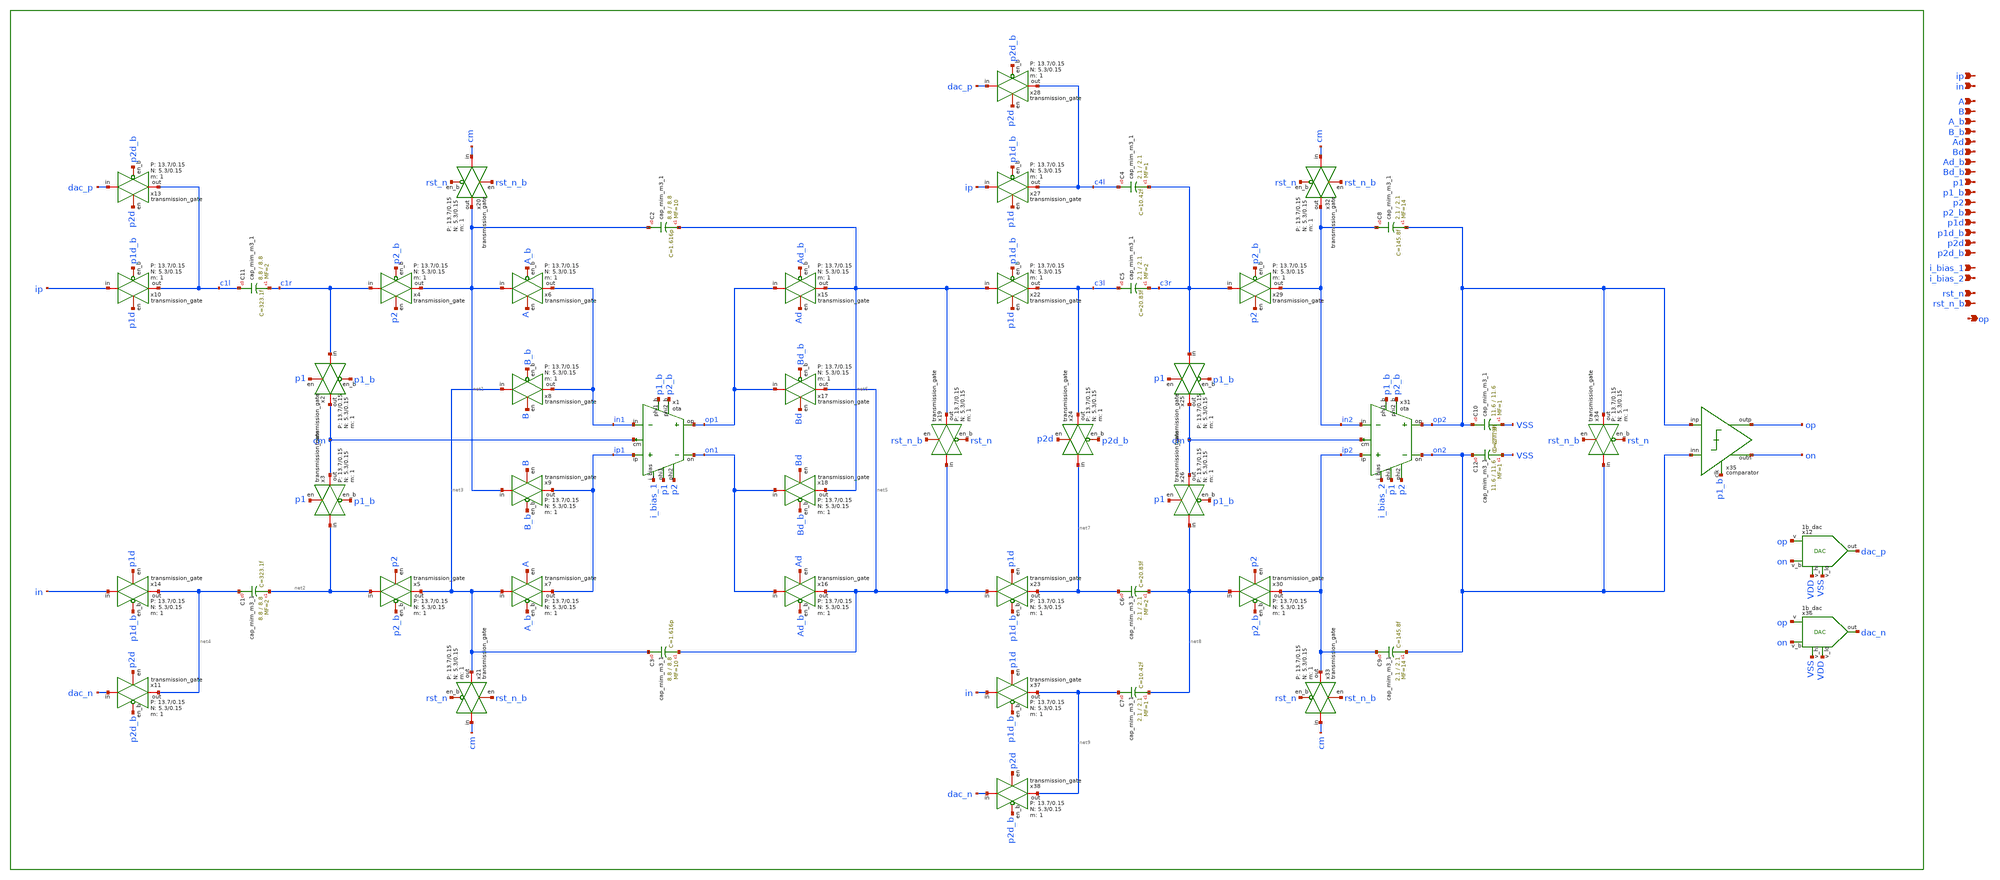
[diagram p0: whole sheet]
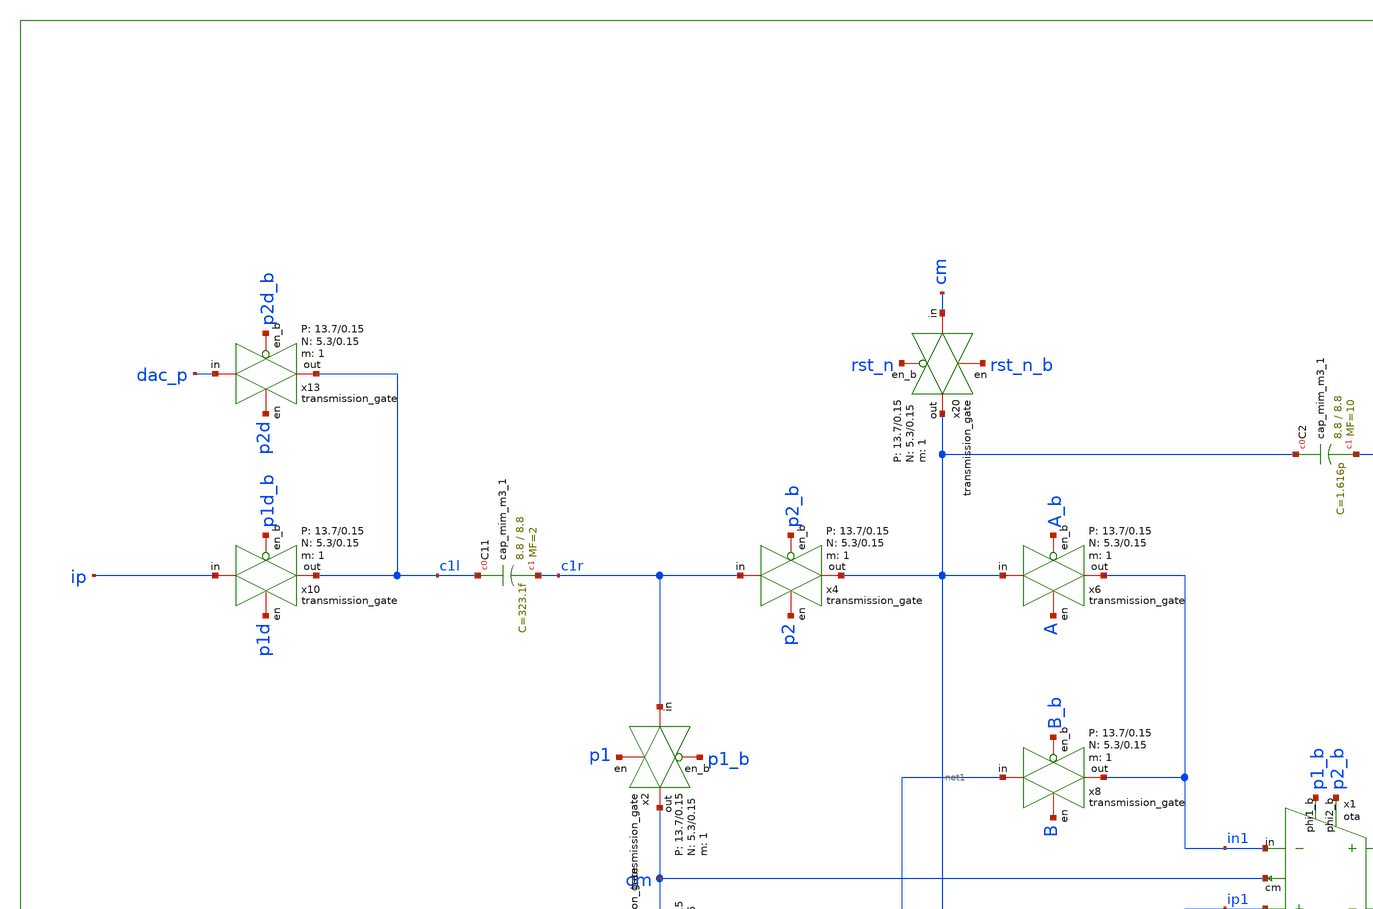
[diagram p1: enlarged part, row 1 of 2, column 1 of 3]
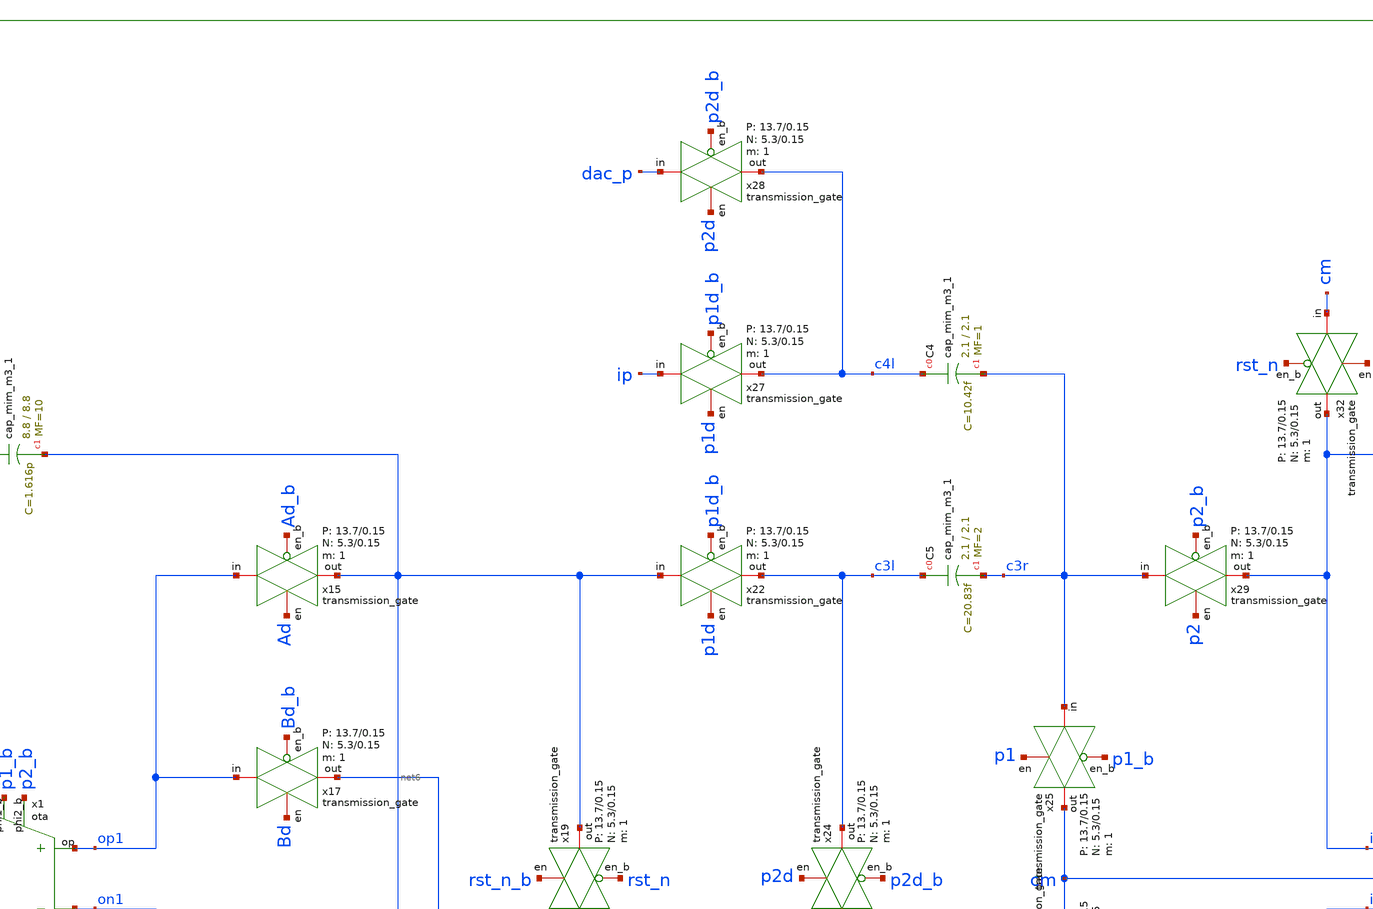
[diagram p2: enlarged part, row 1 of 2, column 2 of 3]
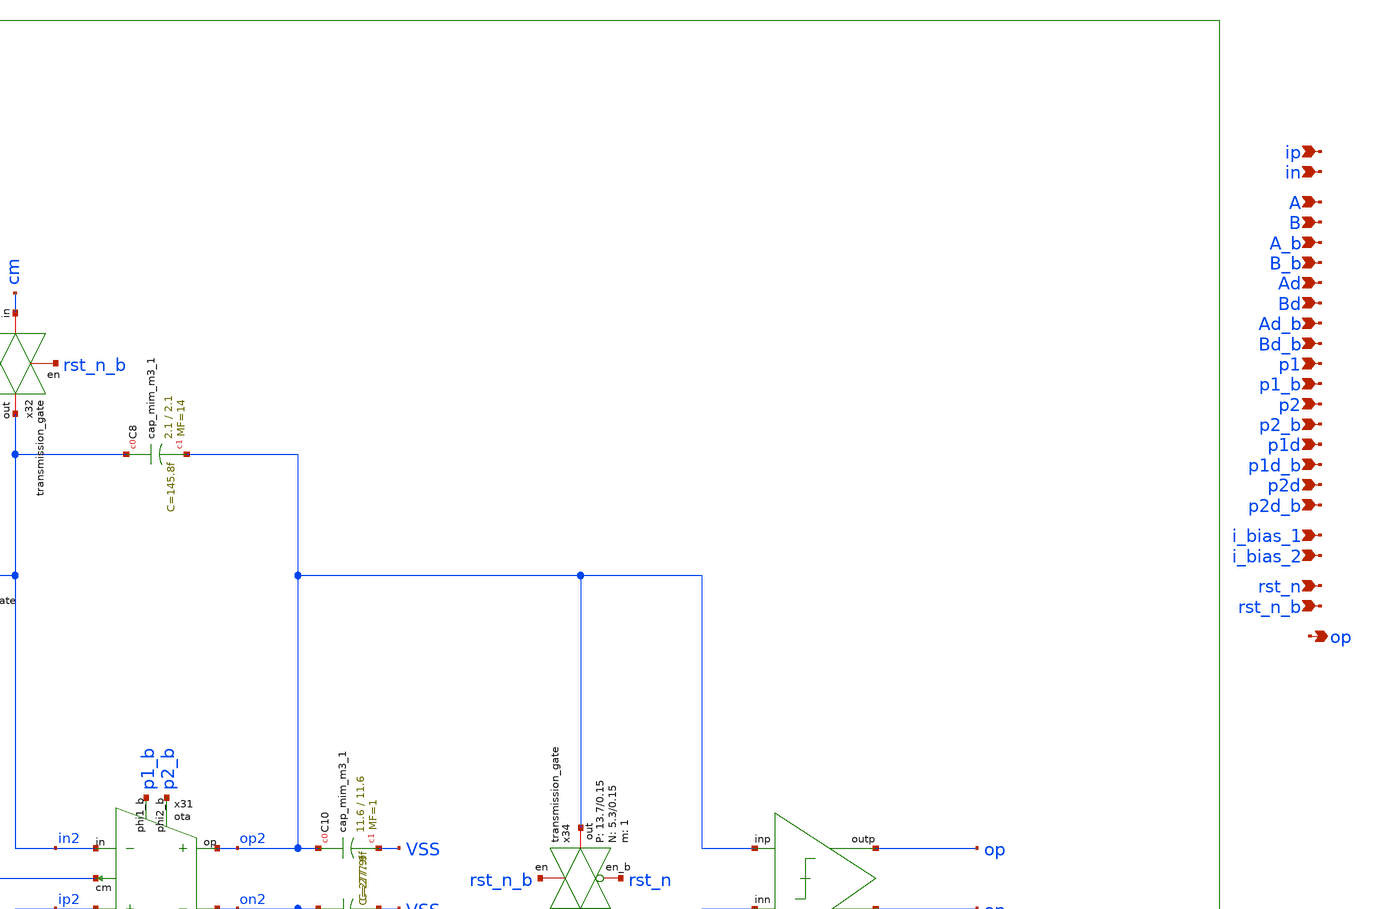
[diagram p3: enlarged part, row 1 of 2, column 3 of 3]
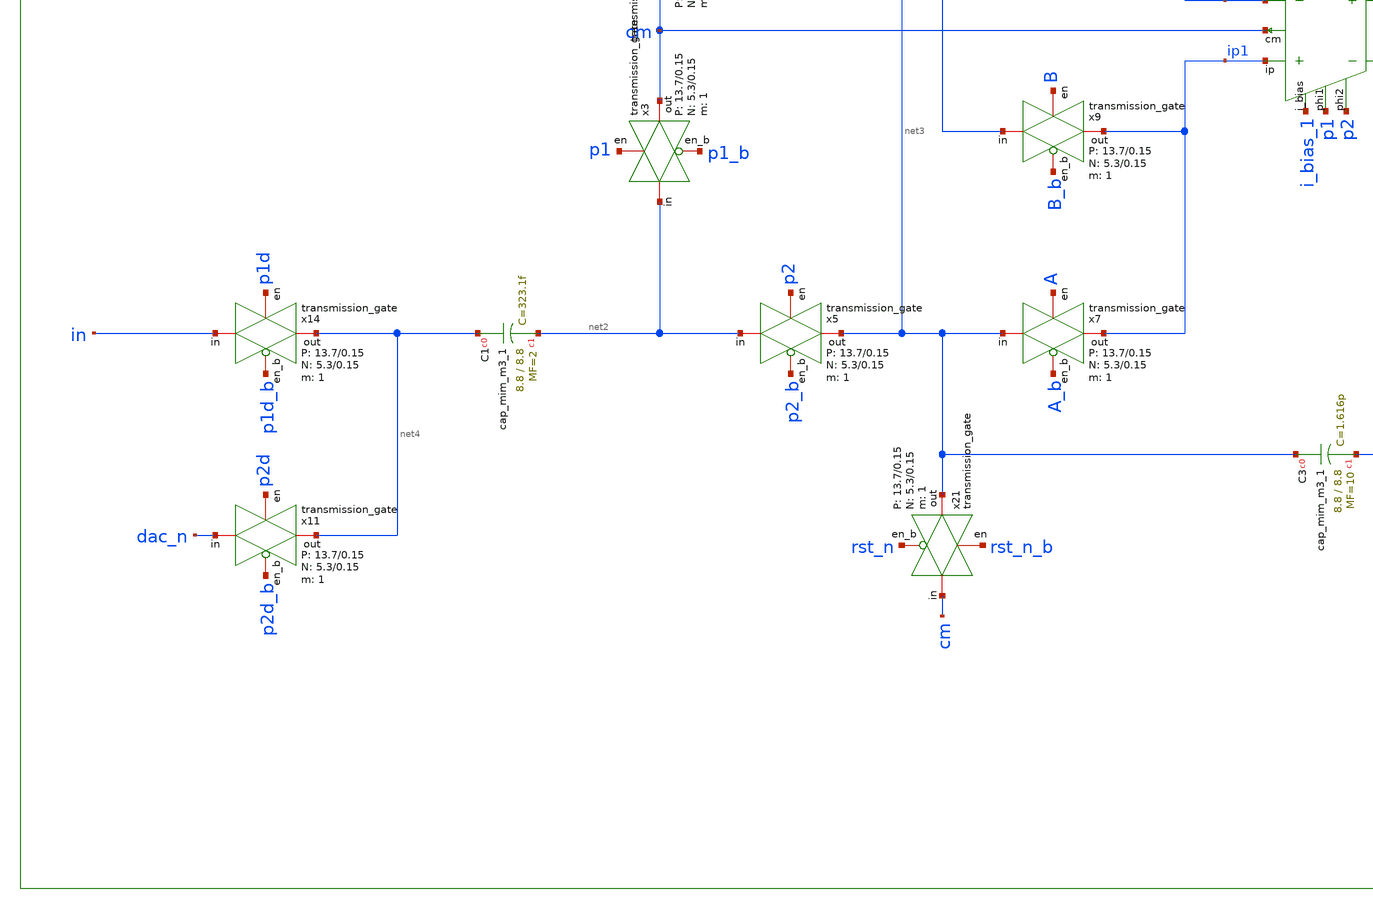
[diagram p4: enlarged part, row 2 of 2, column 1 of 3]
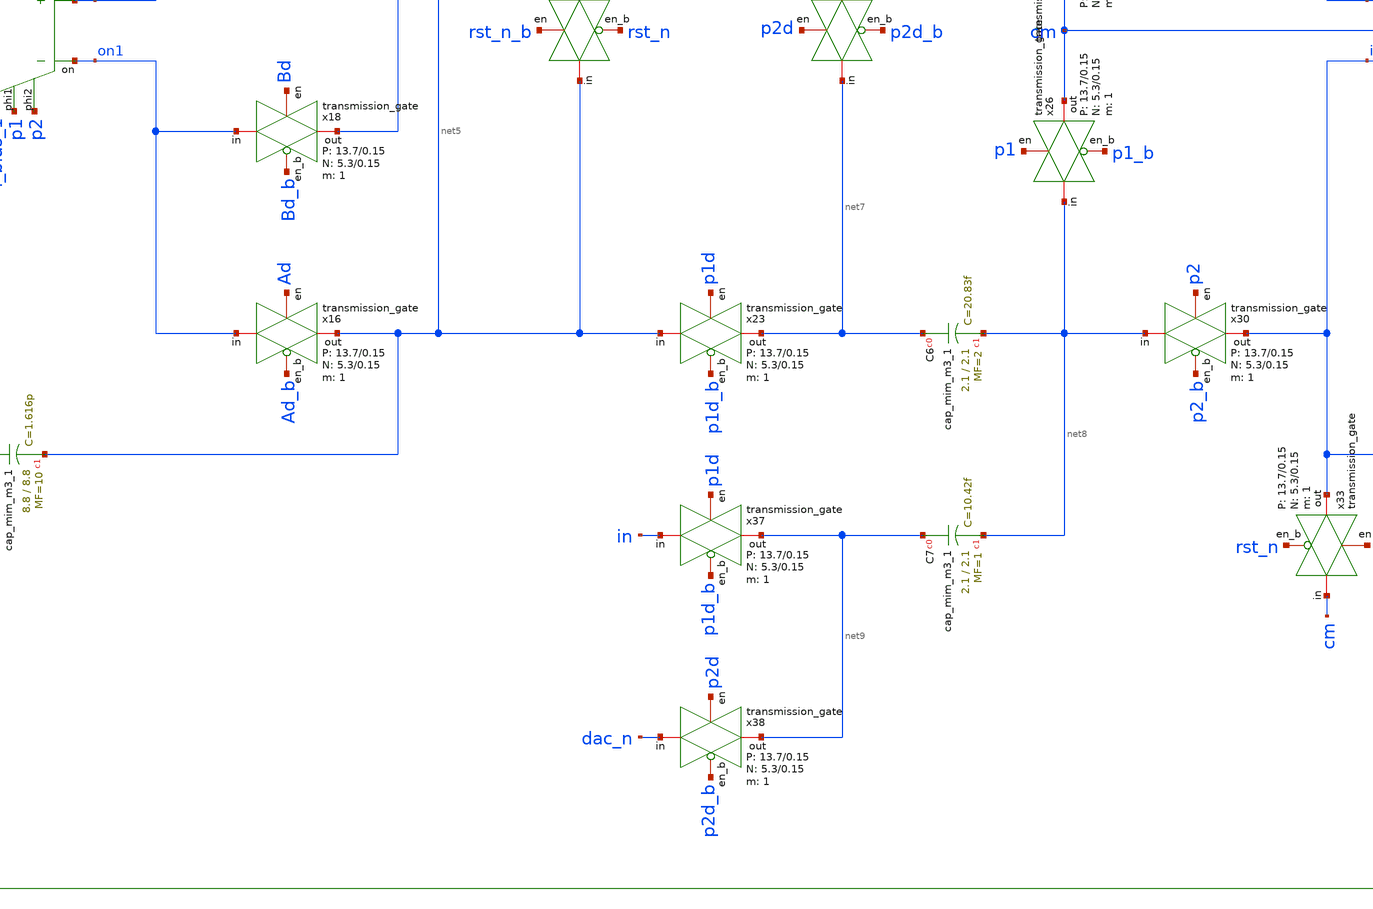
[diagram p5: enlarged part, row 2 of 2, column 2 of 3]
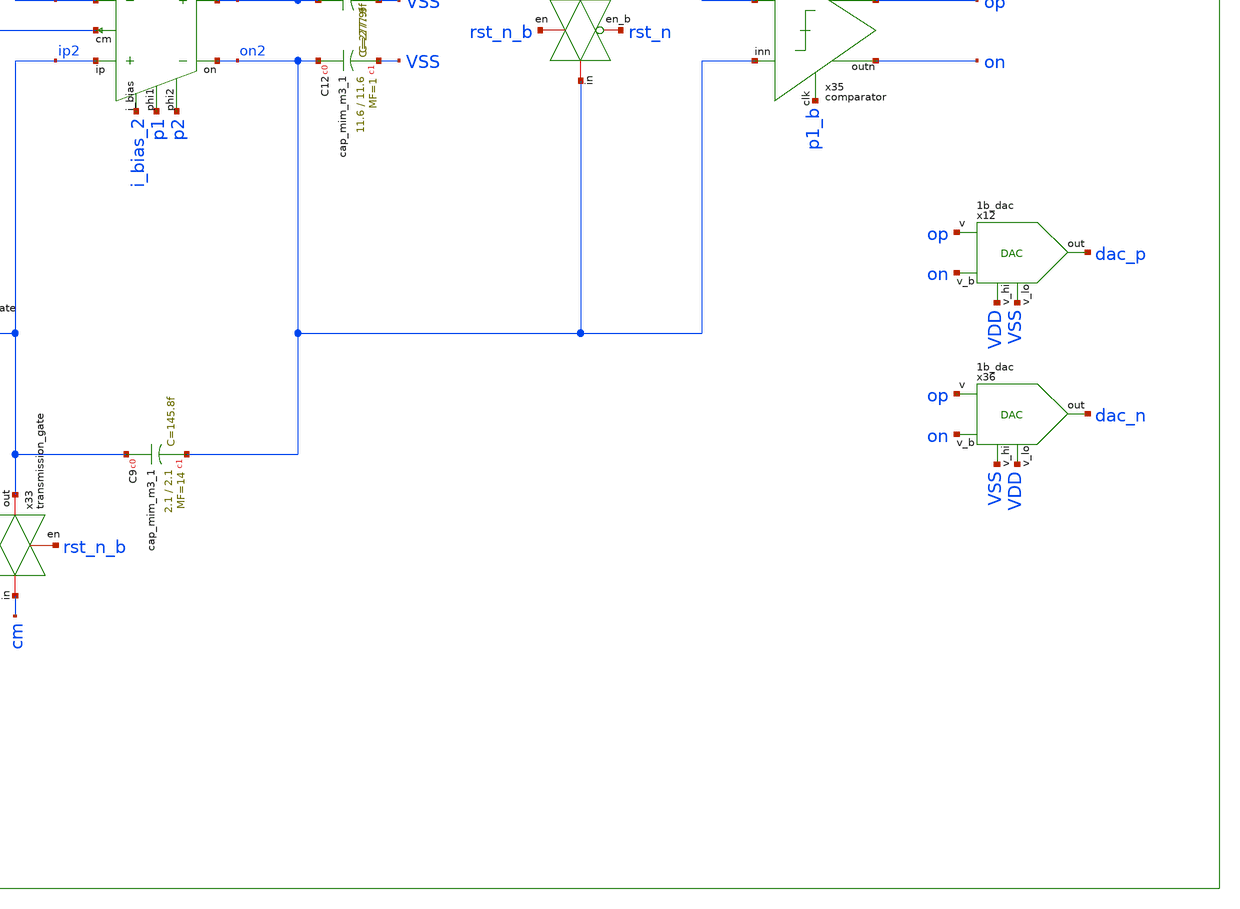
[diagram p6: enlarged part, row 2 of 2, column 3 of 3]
** sch_path: design/analog_modulator/schematic/modulator_backup.sch
**.subckt modulator_backup ip in A B A_b B_b Ad Bd Ad_b Bd_b p1 p1_b p2 p2_b p1d p1d_b p2d p2d_b
*+ i_bias_1 i_bias_2 rst_n rst_n_b op
*.ipin ip
*.ipin in
*.ipin A
*.ipin B
*.ipin A_b
*.ipin B_b
*.ipin Ad
*.ipin Bd
*.ipin Ad_b
*.ipin Bd_b
*.ipin p1
*.ipin p1_b
*.ipin p2
*.ipin p2_b
*.ipin p1d
*.ipin p1d_b
*.ipin p2d
*.ipin p2d_b
*.ipin i_bias_1
*.ipin i_bias_2
*.ipin rst_n
*.ipin rst_n_b
*.opin op
x1 i_bias_1 ip1 in1 p1 p1_b p2 p2_b op1 on1 cm VDD VSS ota
x4 c1r net1 p2 p2_b VDD VSS transmission_gate N=1 W_N=5.3 L_N=0.15 W_P=13.7 L_P=0.15
x5 net2 net3 p2 p2_b VDD VSS transmission_gate N=1 W_N=5.3 L_N=0.15 W_P=13.7 L_P=0.15
x2 c1r cm p1 p1_b VDD VSS transmission_gate N=1 W_N=5.3 L_N=0.15 W_P=13.7 L_P=0.15
x3 net2 cm p1 p1_b VDD VSS transmission_gate N=1 W_N=5.3 L_N=0.15 W_P=13.7 L_P=0.15
x10 ip c1l p1d p1d_b VDD VSS transmission_gate N=1 W_N=5.3 L_N=0.15 W_P=13.7 L_P=0.15
x11 dac_n net4 p2d p2d_b VDD VSS transmission_gate N=1 W_N=5.3 L_N=0.15 W_P=13.7 L_P=0.15
x12 VDD VSS op dac_p on VDD VSS 1b_dac
x13 dac_p c1l p2d p2d_b VDD VSS transmission_gate N=1 W_N=5.3 L_N=0.15 W_P=13.7 L_P=0.15
x14 in net4 p1d p1d_b VDD VSS transmission_gate N=1 W_N=5.3 L_N=0.15 W_P=13.7 L_P=0.15
x19 net5 net6 rst_n_b rst_n VDD VSS transmission_gate N=1 W_N=5.3 L_N=0.15 W_P=13.7 L_P=0.15
x20 cm net1 rst_n_b rst_n VDD VSS transmission_gate N=1 W_N=5.3 L_N=0.15 W_P=13.7 L_P=0.15
x21 cm net3 rst_n_b rst_n VDD VSS transmission_gate N=1 W_N=5.3 L_N=0.15 W_P=13.7 L_P=0.15
x22 net6 c3l p1d p1d_b VDD VSS transmission_gate N=1 W_N=5.3 L_N=0.15 W_P=13.7 L_P=0.15
x23 net5 net7 p1d p1d_b VDD VSS transmission_gate N=1 W_N=5.3 L_N=0.15 W_P=13.7 L_P=0.15
x24 net7 c3l p2d p2d_b VDD VSS transmission_gate N=1 W_N=5.3 L_N=0.15 W_P=13.7 L_P=0.15
x25 c3r cm p1 p1_b VDD VSS transmission_gate N=1 W_N=5.3 L_N=0.15 W_P=13.7 L_P=0.15
x26 net8 cm p1 p1_b VDD VSS transmission_gate N=1 W_N=5.3 L_N=0.15 W_P=13.7 L_P=0.15
x27 ip c4l p1d p1d_b VDD VSS transmission_gate N=1 W_N=5.3 L_N=0.15 W_P=13.7 L_P=0.15
x28 dac_p c4l p2d p2d_b VDD VSS transmission_gate N=1 W_N=5.3 L_N=0.15 W_P=13.7 L_P=0.15
x29 c3r in2 p2 p2_b VDD VSS transmission_gate N=1 W_N=5.3 L_N=0.15 W_P=13.7 L_P=0.15
x30 net8 ip2 p2 p2_b VDD VSS transmission_gate N=1 W_N=5.3 L_N=0.15 W_P=13.7 L_P=0.15
x31 i_bias_2 ip2 in2 p1 p1_b p2 p2_b op2 on2 cm VDD VSS ota
x32 cm in2 rst_n_b rst_n VDD VSS transmission_gate N=1 W_N=5.3 L_N=0.15 W_P=13.7 L_P=0.15
x33 cm ip2 rst_n_b rst_n VDD VSS transmission_gate N=1 W_N=5.3 L_N=0.15 W_P=13.7 L_P=0.15
x34 on2 op2 rst_n_b rst_n VDD VSS transmission_gate N=1 W_N=5.3 L_N=0.15 W_P=13.7 L_P=0.15
x35 op2 on2 op p1_b on VDD VSS comparator
x36 VSS VDD op dac_n on VDD VSS 1b_dac
x37 in net9 p1d p1d_b VDD VSS transmission_gate N=1 W_N=5.3 L_N=0.15 W_P=13.7 L_P=0.15
x38 dac_n net9 p2d p2d_b VDD VSS transmission_gate N=1 W_N=5.3 L_N=0.15 W_P=13.7 L_P=0.15
XC11 c1l c1r sky130_fd_pr__cap_mim_m3_1 W=8.8 L=8.8 MF=2 m=2
XC1 net4 net2 sky130_fd_pr__cap_mim_m3_1 W=8.8 L=8.8 MF=2 m=2
XC2 net1 net6 sky130_fd_pr__cap_mim_m3_1 W=8.8 L=8.8 MF=10 m=10
XC3 net3 net5 sky130_fd_pr__cap_mim_m3_1 W=8.8 L=8.8 MF=10 m=10
XC4 c4l c3r sky130_fd_pr__cap_mim_m3_1 W=2.1 L=2.1 MF=1 m=1
XC5 c3l c3r sky130_fd_pr__cap_mim_m3_1 W=2.1 L=2.1 MF=2 m=2
XC6 net7 net8 sky130_fd_pr__cap_mim_m3_1 W=2.1 L=2.1 MF=2 m=2
XC7 net9 net8 sky130_fd_pr__cap_mim_m3_1 W=2.1 L=2.1 MF=1 m=1
XC8 in2 op2 sky130_fd_pr__cap_mim_m3_1 W=2.1 L=2.1 MF=14 m=14
XC9 ip2 on2 sky130_fd_pr__cap_mim_m3_1 W=2.1 L=2.1 MF=14 m=14
XC10 op2 VSS sky130_fd_pr__cap_mim_m3_1 W=11.6 L=11.6 MF=1 m=1
XC12 on2 VSS sky130_fd_pr__cap_mim_m3_1 W=11.6 L=11.6 MF=1 m=1
x6 net1 in1 A A_b VDD VSS transmission_gate N=1 W_N=5.3 L_N=0.15 W_P=13.7 L_P=0.15
x7 net3 ip1 A A_b VDD VSS transmission_gate N=1 W_N=5.3 L_N=0.15 W_P=13.7 L_P=0.15
x8 net3 in1 B B_b VDD VSS transmission_gate N=1 W_N=5.3 L_N=0.15 W_P=13.7 L_P=0.15
x9 net1 ip1 B B_b VDD VSS transmission_gate N=1 W_N=5.3 L_N=0.15 W_P=13.7 L_P=0.15
x15 op1 net6 Ad Ad_b VDD VSS transmission_gate N=1 W_N=5.3 L_N=0.15 W_P=13.7 L_P=0.15
x16 on1 net5 Ad Ad_b VDD VSS transmission_gate N=1 W_N=5.3 L_N=0.15 W_P=13.7 L_P=0.15
x17 op1 net5 Bd Bd_b VDD VSS transmission_gate N=1 W_N=5.3 L_N=0.15 W_P=13.7 L_P=0.15
x18 on1 net6 Bd Bd_b VDD VSS transmission_gate N=1 W_N=5.3 L_N=0.15 W_P=13.7 L_P=0.15
**.ends
.end
